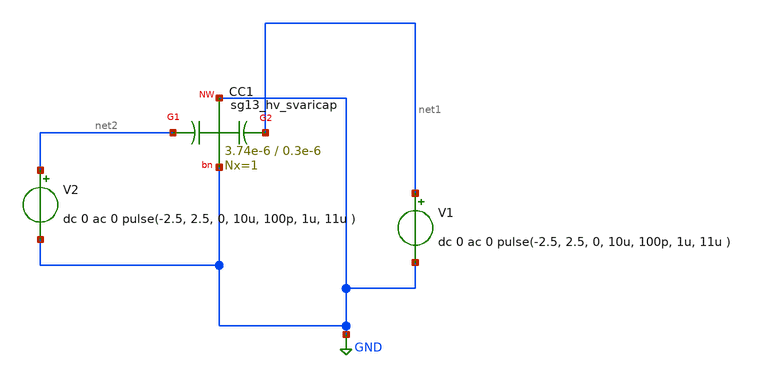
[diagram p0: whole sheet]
** sch_path: ihp-sg13g2/xschem_libs/sg13g2_tests_ase/tran_svaricap_test/schematic/tran_svaricap_test.sch
**.subckt tran_svaricap_test
XC1 net2 GND net1 GND sg13_hv_svaricap w=3.74e-6 l=0.3e-6 Nx=1
V1 net1 GND dc 0 ac 0 pulse(-2.5, 2.5, 0, 10u, 100p, 1u, 11u )
V2 net2 GND dc 0 ac 0 pulse(-2.5, 2.5, 0, 10u, 100p, 1u, 11u )
**.ends
.GLOBAL GND
.end
